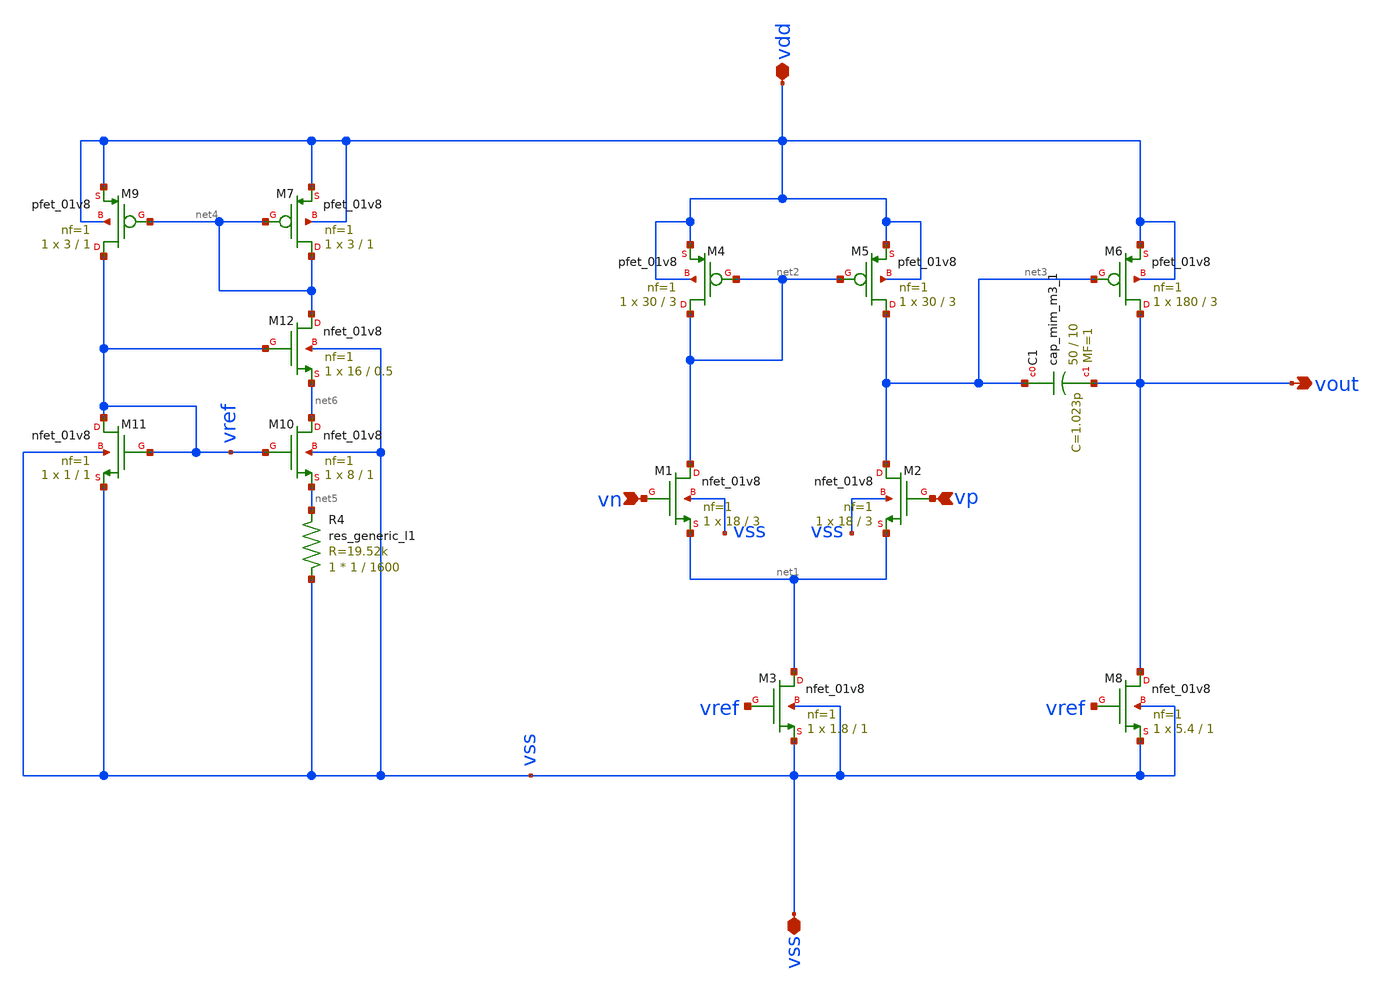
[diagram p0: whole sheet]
** sch_path: analog/library/LDO/test_two_stage.sch
**.subckt test_two_stage vdd vss vn vp vout
*.iopin vdd
*.iopin vss
*.ipin vn
*.ipin vp
*.opin vout
XM1 net2 vn net1 vss sky130_fd_pr__nfet_01v8 L=3 W=18 nf=1 ad='int((nf+1)/2) * W/nf * 0.29' as='int((nf+2)/2) * W/nf * 0.29'
+ pd='2*int((nf+1)/2) * (W/nf + 0.29)' ps='2*int((nf+2)/2) * (W/nf + 0.29)' nrd='0.29 / W' nrs='0.29 / W'
+ sa=0 sb=0 sd=0 mult=1 m=1
XM2 net3 vp net1 vss sky130_fd_pr__nfet_01v8 L=3 W=18 nf=1 ad='int((nf+1)/2) * W/nf * 0.29' as='int((nf+2)/2) * W/nf * 0.29'
+ pd='2*int((nf+1)/2) * (W/nf + 0.29)' ps='2*int((nf+2)/2) * (W/nf + 0.29)' nrd='0.29 / W' nrs='0.29 / W'
+ sa=0 sb=0 sd=0 mult=1 m=1
XM4 net2 net2 vdd vdd sky130_fd_pr__pfet_01v8 L=3 W=30 nf=1 ad='int((nf+1)/2) * W/nf * 0.29' as='int((nf+2)/2) * W/nf * 0.29'
+ pd='2*int((nf+1)/2) * (W/nf + 0.29)' ps='2*int((nf+2)/2) * (W/nf + 0.29)' nrd='0.29 / W' nrs='0.29 / W'
+ sa=0 sb=0 sd=0 mult=1 m=1
XM5 net3 net2 vdd vdd sky130_fd_pr__pfet_01v8 L=3 W=30 nf=1 ad='int((nf+1)/2) * W/nf * 0.29' as='int((nf+2)/2) * W/nf * 0.29'
+ pd='2*int((nf+1)/2) * (W/nf + 0.29)' ps='2*int((nf+2)/2) * (W/nf + 0.29)' nrd='0.29 / W' nrs='0.29 / W'
+ sa=0 sb=0 sd=0 mult=1 m=1
XM6 vout net3 vdd vdd sky130_fd_pr__pfet_01v8 L=3 W=180 nf=1 ad='int((nf+1)/2) * W/nf * 0.29' as='int((nf+2)/2) * W/nf * 0.29'
+ pd='2*int((nf+1)/2) * (W/nf + 0.29)' ps='2*int((nf+2)/2) * (W/nf + 0.29)' nrd='0.29 / W' nrs='0.29 / W'
+ sa=0 sb=0 sd=0 mult=1 m=1
XM3 net1 vref vss vss sky130_fd_pr__nfet_01v8 L=1 W=1.8 nf=1 ad='int((nf+1)/2) * W/nf * 0.29' as='int((nf+2)/2) * W/nf * 0.29'
+ pd='2*int((nf+1)/2) * (W/nf + 0.29)' ps='2*int((nf+2)/2) * (W/nf + 0.29)' nrd='0.29 / W' nrs='0.29 / W'
+ sa=0 sb=0 sd=0 mult=1 m=1
XM8 vout vref vss vss sky130_fd_pr__nfet_01v8 L=1 W=5.4 nf=1 ad='int((nf+1)/2) * W/nf * 0.29' as='int((nf+2)/2) * W/nf * 0.29'
+ pd='2*int((nf+1)/2) * (W/nf + 0.29)' ps='2*int((nf+2)/2) * (W/nf + 0.29)' nrd='0.29 / W' nrs='0.29 / W'
+ sa=0 sb=0 sd=0 mult=1 m=1
XC1 net3 vout sky130_fd_pr__cap_mim_m3_1 W=50 L=10 MF=1 m=1
XM7 net4 net4 vdd vdd sky130_fd_pr__pfet_01v8 L=1 W=3 nf=1 ad='int((1 + 1)/2) * 3 / 1 * 0.29' as='int((1 + 2)/2) * 3 / 1 * 0.29'
+ pd='2*int((1 + 1)/2) * (3 / 1 + 0.29)' ps='2*int((1 + 2)/2) * (3 / 1 + 0.29)' nrd='0.29 / 3 ' nrs='0.29 / 3 '
+ sa=0 sb=0 sd=0 mult=1 m=1
XM9 vref net4 vdd vdd sky130_fd_pr__pfet_01v8 L=1 W=3 nf=1 ad='int((1 + 1)/2) * 3 / 1 * 0.29' as='int((1 + 2)/2) * 3 / 1 * 0.29'
+ pd='2*int((1 + 1)/2) * (3 / 1 + 0.29)' ps='2*int((1 + 2)/2) * (3 / 1 + 0.29)' nrd='0.29 / 3 ' nrs='0.29 / 3 '
+ sa=0 sb=0 sd=0 mult=1 m=1
XM10 net6 vref net5 vss sky130_fd_pr__nfet_01v8 L=1 W=8 nf=1 ad='int((1 + 1)/2) * 8 / 1 * 0.29' as='int((1 + 2)/2) * 8 / 1 * 0.29'
+ pd='2*int((1 + 1)/2) * (8 / 1 + 0.29)' ps='2*int((1 + 2)/2) * (8 / 1 + 0.29)' nrd='0.29 / 8 ' nrs='0.29 / 8 '
+ sa=0 sb=0 sd=0 mult=1 m=1
XM11 vref vref vss vss sky130_fd_pr__nfet_01v8 L=1 W=1 nf=1 ad='int((1 + 1)/2) * 1 / 1 * 0.29' as='int((1 + 2)/2) * 1 / 1 * 0.29'
+ pd='2*int((1 + 1)/2) * (1 / 1 + 0.29)' ps='2*int((1 + 2)/2) * (1 / 1 + 0.29)' nrd='0.29 / 1 ' nrs='0.29 / 1 '
+ sa=0 sb=0 sd=0 mult=1 m=1
R4 vss net5 sky130_fd_pr__res_generic_l1 W=1 L=1600 m=1
XM12 net4 vref net6 vss sky130_fd_pr__nfet_01v8 L=0.5 W=16 nf=1 ad='int((1 + 1)/2) * 16 / 1 * 0.29' as='int((1 + 2)/2) * 16 / 1 * 0.29'
+ pd='2*int((1 + 1)/2) * (16 / 1 + 0.29)' ps='2*int((1 + 2)/2) * (16 / 1 + 0.29)' nrd='0.29 / 16 ' nrs='0.29 / 16 '
+ sa=0 sb=0 sd=0 mult=1 m=1
**.ends
.end
